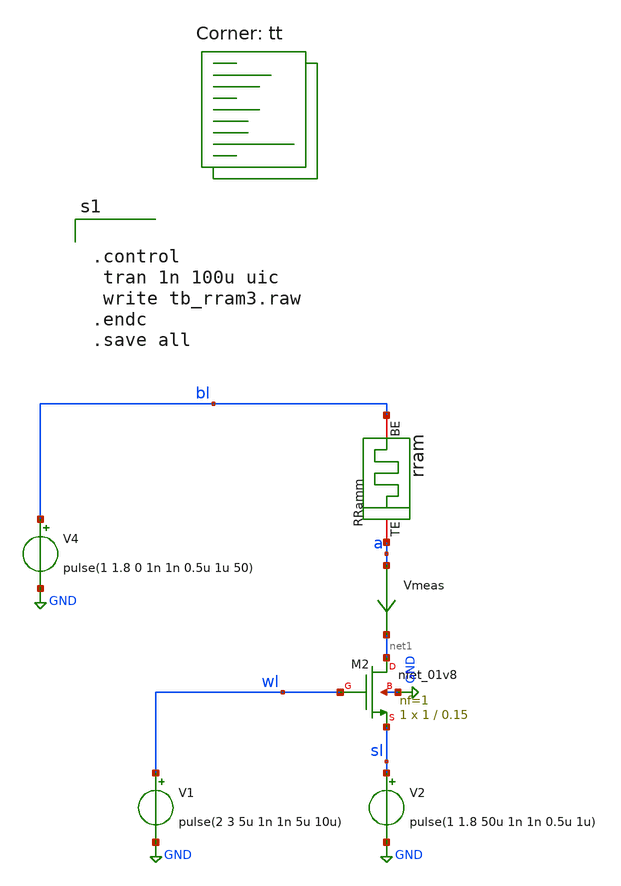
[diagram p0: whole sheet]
** sch_path: designs/tb_memristor/tb_rram3.sch
**.subckt tb_rram3
V4 bl GND pulse(1 1.8 0 1n 1n 0.5u 1u 50)
XM2 net1 wl sl GND sky130_fd_pr__nfet_01v8 L=0.15 W=1 nf=1 ad='int((1 + 1)/2) * 1 / 1 * 0.29' as='int((1 + 2)/2) * 1 / 1 * 0.29'
+ pd='2*int((1 + 1)/2) * (1 / 1 + 0.29)' ps='2*int((1 + 2)/2) * (1 / 1 + 0.29)' nrd='0.29 / 1 ' nrs='0.29 / 1 '
+ sa=0 sb=0 sd=0 mult=1 m=1
V1 wl GND pulse(2 3 5u 1n 1n 5u 10u)
V2 sl GND pulse(1 1.8 50u 1n 1n 0.5u 1u)
Vmeas a net1 0
.save i(vmeas)
RRamm a bl rram_cell
**** begin user architecture code
.lib $::SKYWATER_MODELS/sky130.lib.spice tt


.control
 tran 1n 100u uic
 write tb_rram3.raw
.endc
.save all

**** end user architecture code
**.ends
.GLOBAL GND
**** begin user architecture code

.subckt rram_cell BE TE
N1 BE TE rram_model
.ends rram_cell

.model rram_model rram_va

.control
pre_osdi /foss/designs/spike_130/designs/memristors/rram_v0_2/rram.osdi
.endc


**** end user architecture code
.end
